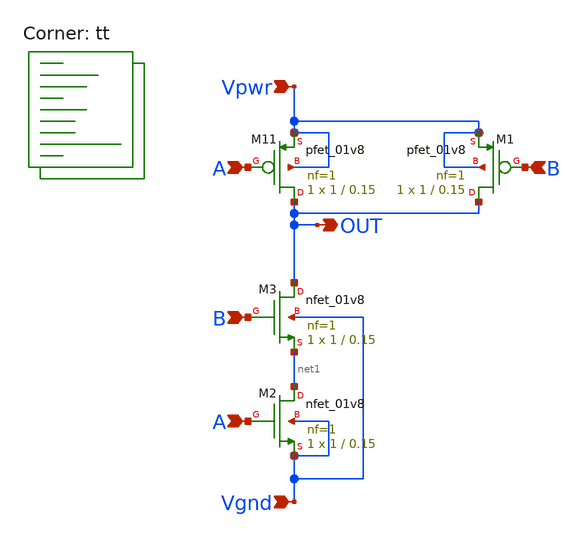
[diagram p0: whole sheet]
** sch_path: MUXDFF/Gates/NAND/nand.sch
**.subckt nand OUT Vpwr Vgnd A B B A
*.opin OUT
*.ipin Vpwr
*.ipin Vgnd
*.ipin A
*.ipin B
*.ipin B
*.ipin A
XM2 net1 A Vgnd Vgnd sky130_fd_pr__nfet_01v8 L=0.15 W=1 nf=1 ad='int((1 + 1)/2) * 1 / 1 * 0.29' as='int((1 + 2)/2) * 1 / 1 * 0.29'
+ pd='2*int((1 + 1)/2) * (1 / 1 + 0.29)' ps='2*int((1 + 2)/2) * (1 / 1 + 0.29)' nrd='0.29 / 1 ' nrs='0.29 / 1 '
+ sa=0 sb=0 sd=0 mult=1 m=1
XM11 OUT A Vpwr Vpwr sky130_fd_pr__pfet_01v8 L=0.15 W=1 nf=1 ad='int((nf+1)/2) * W/nf * 0.29' as='int((nf+2)/2) * W/nf * 0.29'
+ pd='2*int((nf+1)/2) * (W/nf + 0.29)' ps='2*int((nf+2)/2) * (W/nf + 0.29)' nrd='0.29 / W' nrs='0.29 / W'
+ sa=0 sb=0 sd=0 mult=1 m=1
XM1 OUT B Vpwr Vpwr sky130_fd_pr__pfet_01v8 L=0.15 W=1 nf=1 ad='int((nf+1)/2) * W/nf * 0.29' as='int((nf+2)/2) * W/nf * 0.29'
+ pd='2*int((nf+1)/2) * (W/nf + 0.29)' ps='2*int((nf+2)/2) * (W/nf + 0.29)' nrd='0.29 / W' nrs='0.29 / W'
+ sa=0 sb=0 sd=0 mult=1 m=1
XM3 OUT B net1 Vgnd sky130_fd_pr__nfet_01v8 L=0.15 W=1 nf=1 ad='int((1 + 1)/2) * 1 / 1 * 0.29' as='int((1 + 2)/2) * 1 / 1 * 0.29'
+ pd='2*int((1 + 1)/2) * (1 / 1 + 0.29)' ps='2*int((1 + 2)/2) * (1 / 1 + 0.29)' nrd='0.29 / 1 ' nrs='0.29 / 1 '
+ sa=0 sb=0 sd=0 mult=1 m=1
**** begin user architecture code
.lib $::SKYWATER_MODELS/sky130.lib.spice tt
**** end user architecture code
**.ends
.end
